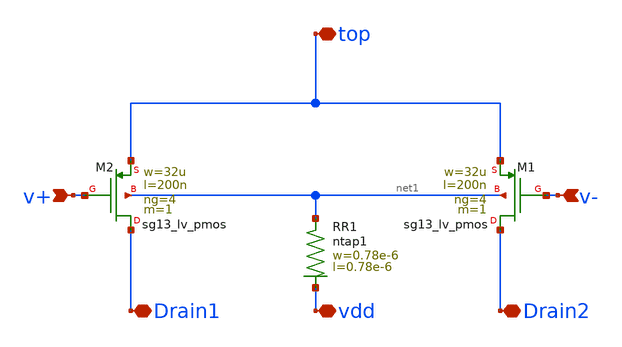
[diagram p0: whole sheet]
** sch_path: modules/module_3_8_bit_SAR_ADC/part_5_layout/components/comparator/layout/input_pair/schematic_mod/input_pair_cm.sch
**.subckt input_pair_cm v+ v- Drain2 Drain1 vdd top
*.ipin v+
*.ipin v-
*.iopin Drain2
*.iopin Drain1
*.iopin vdd
*.iopin top
XM2 Drain1 v+ top net1 sg13_lv_pmos w=32u l=200n ng=4 m=1 mm_ok=1
XM1 Drain2 v- top net1 sg13_lv_pmos w=32u l=200n ng=4 m=1 mm_ok=1
XR1 net1 vdd ntap1 R=262.8 w=0.78e-6 l=0.78e-6
**.ends
.end
